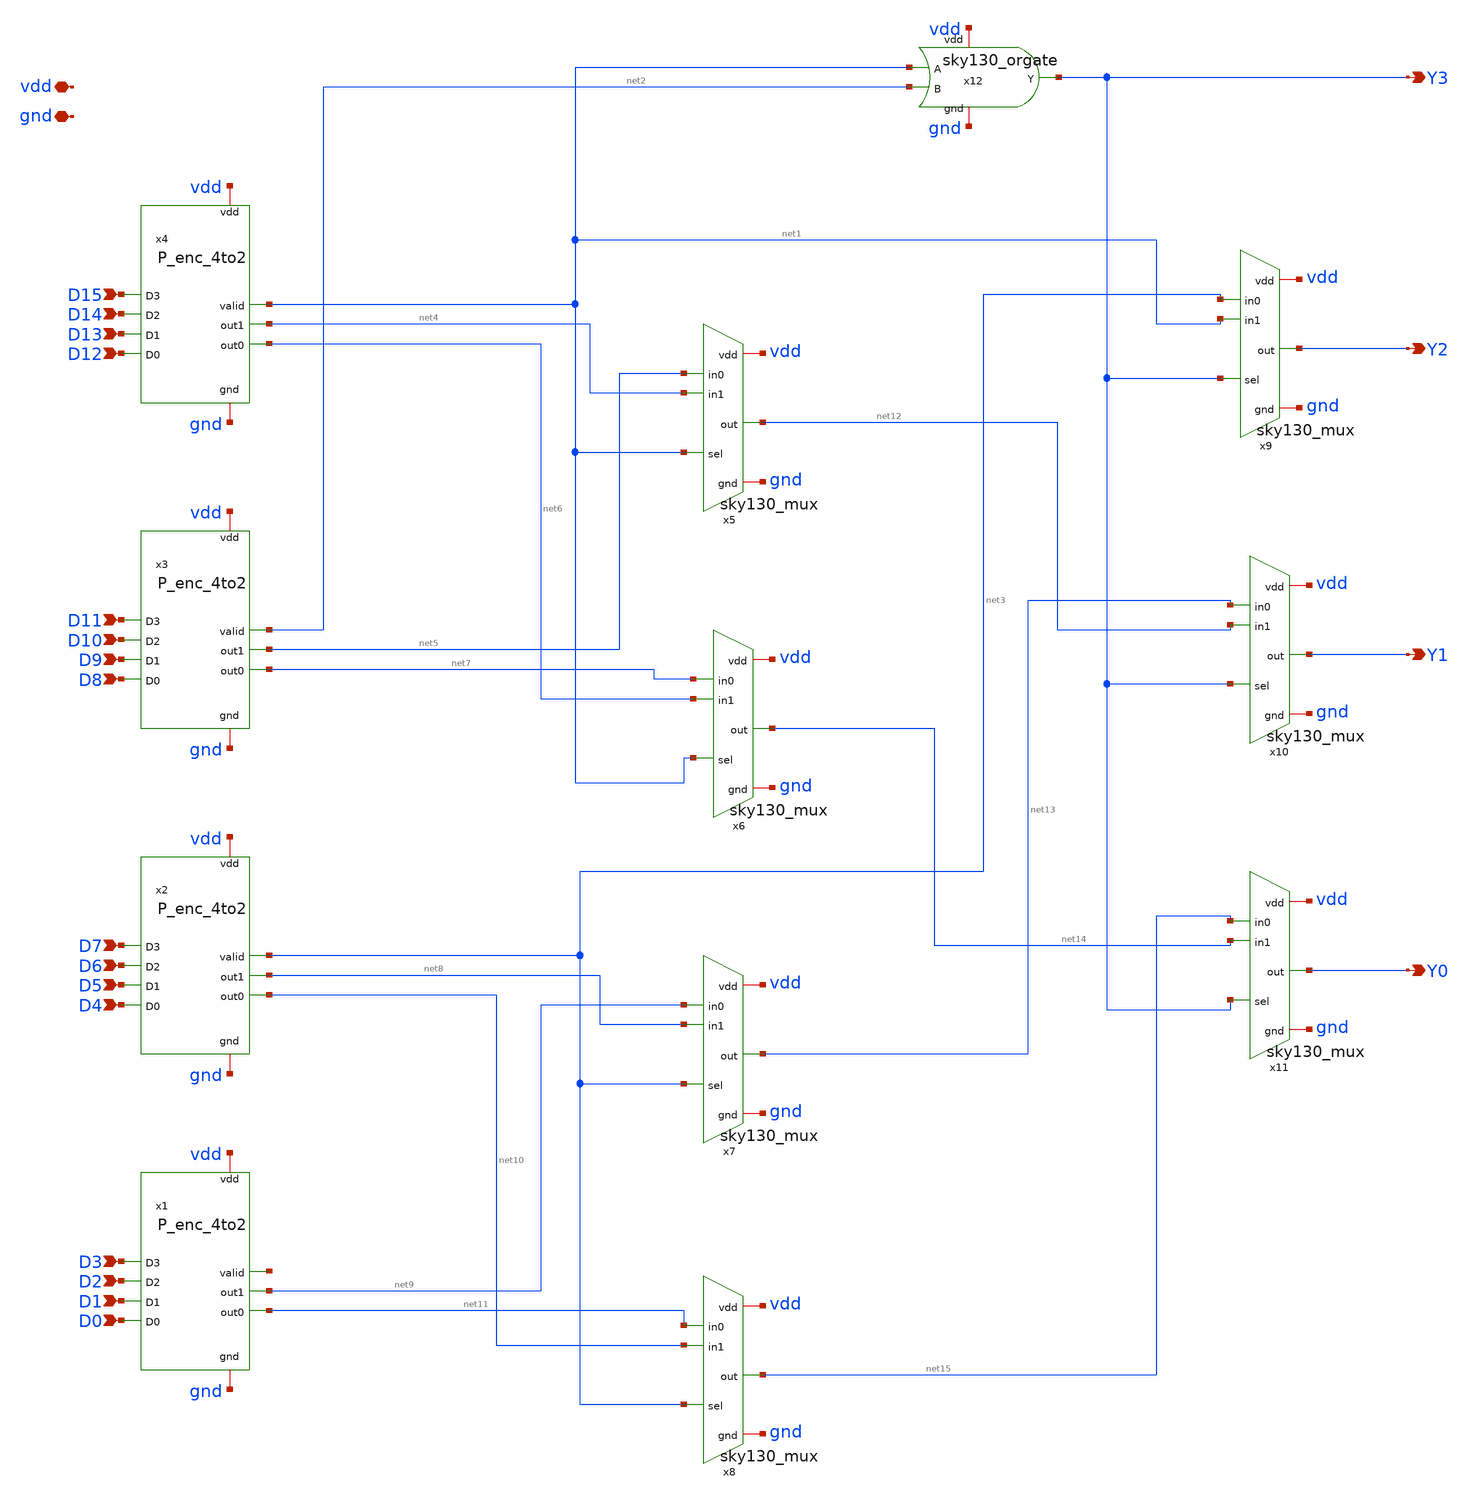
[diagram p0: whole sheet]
** sch_path: Primitives/Priority Encoder 16to4/Xschem Files/P_enc_16to4.sch
**.subckt P_enc_16to4 vdd gnd D0 D1 D2 D3 D4 D5 D6 D7 D8 D9 D10 D11 D12 D13 D14 D15 Y0 Y1 Y2 Y3
*.iopin vdd
*.iopin gnd
*.ipin D0
*.ipin D1
*.ipin D2
*.ipin D3
*.ipin D4
*.ipin D5
*.ipin D6
*.ipin D7
*.ipin D8
*.ipin D9
*.ipin D10
*.ipin D11
*.ipin D12
*.ipin D13
*.ipin D14
*.ipin D15
*.opin Y0
*.opin Y1
*.opin Y2
*.opin Y3
x5 net5 vdd gnd net12 net4 net1 sky130_mux
x6 net7 vdd gnd net14 net6 net1 sky130_mux
x7 net9 vdd gnd net13 net8 net3 sky130_mux
x8 net11 vdd gnd net15 net10 net3 sky130_mux
x9 net3 vdd gnd Y2 net1 Y3 sky130_mux
x10 net13 vdd gnd Y1 net12 Y3 sky130_mux
x11 net15 vdd gnd Y0 net14 Y3 sky130_mux
x12 vdd net1 net2 Y3 gnd sky130_orgate
x3 vdd D11 D10 D9 D8 net7 net2 net5 gnd P_enc_4to2
x2 vdd D7 D6 D5 D4 net10 net3 net8 gnd P_enc_4to2
x1 vdd D3 D2 D1 D0 net11 net16 net9 gnd P_enc_4to2
x4 vdd D15 D14 D13 D12 net6 net1 net4 gnd P_enc_4to2
**.ends

* expanding   symbol:  /home/rachtih/ADC trials/mux/sky130_mux.sym # of pins=6
** sym_path: Primitives/Multiplexer 2to1/Xschem Files/sky130_mux.sym
** sch_path: Primitives/Multiplexer 2to1/Xschem Files/sky130_mux.sch
.subckt sky130_mux in0 vdd gnd out in1 sel
*.iopin vdd
*.iopin gnd
*.ipin in0
*.ipin sel
*.ipin in1
*.opin out
XM1 net1 sel gnd gnd sky130_fd_pr__nfet_01v8 L=0.15 W=1 nf=1 ad='int((1 + 1)/2) * 1 / 1 * 0.29' as='int((1 + 2)/2) * 1 / 1 * 0.29'
+ pd='2*int((1 + 1)/2) * (1 / 1 + 0.29)' ps='2*int((1 + 2)/2) * (1 / 1 + 0.29)' nrd='0.29 / 1 ' nrs='0.29 / 1 '
+ sa=0 sb=0 sd=0 mult=1 m=1
XM2 net1 sel vdd vdd sky130_fd_pr__pfet_01v8 L=0.15 W=1 nf=1 ad='int((1 + 1)/2) * 1 / 1 * 0.29' as='int((1 + 2)/2) * 1 / 1 * 0.29'
+ pd='2*int((1 + 1)/2) * (1 / 1 + 0.29)' ps='2*int((1 + 2)/2) * (1 / 1 + 0.29)' nrd='0.29 / 1 ' nrs='0.29 / 1 '
+ sa=0 sb=0 sd=0 mult=1 m=1
XM3 in1 sel out gnd sky130_fd_pr__nfet_01v8 L=0.15 W=1 nf=1 ad='int((1 + 1)/2) * 1 / 1 * 0.29' as='int((1 + 2)/2) * 1 / 1 * 0.29'
+ pd='2*int((1 + 1)/2) * (1 / 1 + 0.29)' ps='2*int((1 + 2)/2) * (1 / 1 + 0.29)' nrd='0.29 / 1 ' nrs='0.29 / 1 '
+ sa=0 sb=0 sd=0 mult=1 m=1
XM4 in1 net1 out vdd sky130_fd_pr__pfet_01v8 L=0.15 W=1 nf=1 ad='int((1 + 1)/2) * 1 / 1 * 0.29' as='int((1 + 2)/2) * 1 / 1 * 0.29'
+ pd='2*int((1 + 1)/2) * (1 / 1 + 0.29)' ps='2*int((1 + 2)/2) * (1 / 1 + 0.29)' nrd='0.29 / 1 ' nrs='0.29 / 1 '
+ sa=0 sb=0 sd=0 mult=1 m=1
XM5 in0 net1 out gnd sky130_fd_pr__nfet_01v8 L=0.15 W=1 nf=1 ad='int((1 + 1)/2) * 1 / 1 * 0.29' as='int((1 + 2)/2) * 1 / 1 * 0.29'
+ pd='2*int((1 + 1)/2) * (1 / 1 + 0.29)' ps='2*int((1 + 2)/2) * (1 / 1 + 0.29)' nrd='0.29 / 1 ' nrs='0.29 / 1 '
+ sa=0 sb=0 sd=0 mult=1 m=1
XM6 in0 sel out vdd sky130_fd_pr__pfet_01v8 L=0.15 W=1 nf=1 ad='int((1 + 1)/2) * 1 / 1 * 0.29' as='int((1 + 2)/2) * 1 / 1 * 0.29'
+ pd='2*int((1 + 1)/2) * (1 / 1 + 0.29)' ps='2*int((1 + 2)/2) * (1 / 1 + 0.29)' nrd='0.29 / 1 ' nrs='0.29 / 1 '
+ sa=0 sb=0 sd=0 mult=1 m=1
.ends


* expanding   symbol:  /home/rachtih/ADC trials/or_gate/sky130_orgate.sym # of pins=5
** sym_path: Primitives/OR Gate/Xschem Files/sky130_orgate.sym
** sch_path: Primitives/OR Gate/Xschem Files/sky130_orgate.sch
.subckt sky130_orgate vdd A B Y gnd
*.ipin A
*.ipin B
*.iopin gnd
*.iopin vdd
*.opin Y
XM1 net1 B gnd gnd sky130_fd_pr__nfet_01v8 L=0.15 W=1 nf=1 ad='int((1 + 1)/2) * 1 / 1 * 0.29' as='int((1 + 2)/2) * 1 / 1 * 0.29'
+ pd='2*int((1 + 1)/2) * (1 / 1 + 0.29)' ps='2*int((1 + 2)/2) * (1 / 1 + 0.29)' nrd='0.29 / 1 ' nrs='0.29 / 1 '
+ sa=0 sb=0 sd=0 mult=1 m=1
XM2 net2 A vdd vdd sky130_fd_pr__pfet_01v8 L=0.15 W=1 nf=1 ad='int((1 + 1)/2) * 1 / 1 * 0.29' as='int((1 + 2)/2) * 1 / 1 * 0.29'
+ pd='2*int((1 + 1)/2) * (1 / 1 + 0.29)' ps='2*int((1 + 2)/2) * (1 / 1 + 0.29)' nrd='0.29 / 1 ' nrs='0.29 / 1 '
+ sa=0 sb=0 sd=0 mult=1 m=1
XM3 net1 A gnd gnd sky130_fd_pr__nfet_01v8 L=0.15 W=1 nf=1 ad='int((1 + 1)/2) * 1 / 1 * 0.29' as='int((1 + 2)/2) * 1 / 1 * 0.29'
+ pd='2*int((1 + 1)/2) * (1 / 1 + 0.29)' ps='2*int((1 + 2)/2) * (1 / 1 + 0.29)' nrd='0.29 / 1 ' nrs='0.29 / 1 '
+ sa=0 sb=0 sd=0 mult=1 m=1
XM4 net1 B net2 vdd sky130_fd_pr__pfet_01v8 L=0.15 W=1 nf=1 ad='int((1 + 1)/2) * 1 / 1 * 0.29' as='int((1 + 2)/2) * 1 / 1 * 0.29'
+ pd='2*int((1 + 1)/2) * (1 / 1 + 0.29)' ps='2*int((1 + 2)/2) * (1 / 1 + 0.29)' nrd='0.29 / 1 ' nrs='0.29 / 1 '
+ sa=0 sb=0 sd=0 mult=1 m=1
XM5 Y net1 vdd vdd sky130_fd_pr__pfet_01v8 L=0.15 W=1 nf=1 ad='int((1 + 1)/2) * 1 / 1 * 0.29' as='int((1 + 2)/2) * 1 / 1 * 0.29'
+ pd='2*int((1 + 1)/2) * (1 / 1 + 0.29)' ps='2*int((1 + 2)/2) * (1 / 1 + 0.29)' nrd='0.29 / 1 ' nrs='0.29 / 1 '
+ sa=0 sb=0 sd=0 mult=1 m=1
XM6 Y net1 gnd gnd sky130_fd_pr__nfet_01v8 L=0.15 W=1 nf=1 ad='int((1 + 1)/2) * 1 / 1 * 0.29' as='int((1 + 2)/2) * 1 / 1 * 0.29'
+ pd='2*int((1 + 1)/2) * (1 / 1 + 0.29)' ps='2*int((1 + 2)/2) * (1 / 1 + 0.29)' nrd='0.29 / 1 ' nrs='0.29 / 1 '
+ sa=0 sb=0 sd=0 mult=1 m=1
.ends


* expanding   symbol:  /home/rachtih/ADC trials/P_enc/P_enc_4to2.sym # of pins=9
** sym_path: Primitives/Priority Encoder 4to2/Xschem Files/P_enc_4to2.sym
** sch_path: Primitives/Priority Encoder 4to2/Xschem Files/P_enc_4to2.sch
.subckt P_enc_4to2 vdd D3 D2 D1 D0 out0 valid out1 gnd
*.opin valid
*.iopin vdd
*.iopin gnd
*.opin out1
*.opin out0
*.ipin D3
*.ipin D2
*.ipin D1
*.ipin D0
XM5 net7 D3 vdd vdd sky130_fd_pr__pfet_01v8 L=0.15 W=1 nf=1 ad='int((1 + 1)/2) * 1 / 1 * 0.29' as='int((1 + 2)/2) * 1 / 1 * 0.29'
+ pd='2*int((1 + 1)/2) * (1 / 1 + 0.29)' ps='2*int((1 + 2)/2) * (1 / 1 + 0.29)' nrd='0.29 / 1 ' nrs='0.29 / 1 '
+ sa=0 sb=0 sd=0 mult=1 m=1
XM6 net8 D2 net7 vdd sky130_fd_pr__pfet_01v8 L=0.15 W=1 nf=1 ad='int((1 + 1)/2) * 1 / 1 * 0.29' as='int((1 + 2)/2) * 1 / 1 * 0.29'
+ pd='2*int((1 + 1)/2) * (1 / 1 + 0.29)' ps='2*int((1 + 2)/2) * (1 / 1 + 0.29)' nrd='0.29 / 1 ' nrs='0.29 / 1 '
+ sa=0 sb=0 sd=0 mult=1 m=1
XM7 net9 D1 net8 vdd sky130_fd_pr__pfet_01v8 L=0.15 W=1 nf=1 ad='int((1 + 1)/2) * 1 / 1 * 0.29' as='int((1 + 2)/2) * 1 / 1 * 0.29'
+ pd='2*int((1 + 1)/2) * (1 / 1 + 0.29)' ps='2*int((1 + 2)/2) * (1 / 1 + 0.29)' nrd='0.29 / 1 ' nrs='0.29 / 1 '
+ sa=0 sb=0 sd=0 mult=1 m=1
XM8 net1 D0 net9 vdd sky130_fd_pr__pfet_01v8 L=0.15 W=1 nf=1 ad='int((1 + 1)/2) * 1 / 1 * 0.29' as='int((1 + 2)/2) * 1 / 1 * 0.29'
+ pd='2*int((1 + 1)/2) * (1 / 1 + 0.29)' ps='2*int((1 + 2)/2) * (1 / 1 + 0.29)' nrd='0.29 / 1 ' nrs='0.29 / 1 '
+ sa=0 sb=0 sd=0 mult=1 m=1
XM9 net1 D0 gnd gnd sky130_fd_pr__nfet_01v8 L=0.15 W=1 nf=1 ad='int((1 + 1)/2) * 1 / 1 * 0.29' as='int((1 + 2)/2) * 1 / 1 * 0.29'
+ pd='2*int((1 + 1)/2) * (1 / 1 + 0.29)' ps='2*int((1 + 2)/2) * (1 / 1 + 0.29)' nrd='0.29 / 1 ' nrs='0.29 / 1 '
+ sa=0 sb=0 sd=0 mult=1 m=1
XM10 net1 D1 gnd gnd sky130_fd_pr__nfet_01v8 L=0.15 W=1 nf=1 ad='int((1 + 1)/2) * 1 / 1 * 0.29' as='int((1 + 2)/2) * 1 / 1 * 0.29'
+ pd='2*int((1 + 1)/2) * (1 / 1 + 0.29)' ps='2*int((1 + 2)/2) * (1 / 1 + 0.29)' nrd='0.29 / 1 ' nrs='0.29 / 1 '
+ sa=0 sb=0 sd=0 mult=1 m=1
XM11 net1 D2 gnd gnd sky130_fd_pr__nfet_01v8 L=0.15 W=1 nf=1 ad='int((1 + 1)/2) * 1 / 1 * 0.29' as='int((1 + 2)/2) * 1 / 1 * 0.29'
+ pd='2*int((1 + 1)/2) * (1 / 1 + 0.29)' ps='2*int((1 + 2)/2) * (1 / 1 + 0.29)' nrd='0.29 / 1 ' nrs='0.29 / 1 '
+ sa=0 sb=0 sd=0 mult=1 m=1
XM12 net1 D3 gnd gnd sky130_fd_pr__nfet_01v8 L=0.15 W=1 nf=1 ad='int((1 + 1)/2) * 1 / 1 * 0.29' as='int((1 + 2)/2) * 1 / 1 * 0.29'
+ pd='2*int((1 + 1)/2) * (1 / 1 + 0.29)' ps='2*int((1 + 2)/2) * (1 / 1 + 0.29)' nrd='0.29 / 1 ' nrs='0.29 / 1 '
+ sa=0 sb=0 sd=0 mult=1 m=1
XM13 valid net1 gnd gnd sky130_fd_pr__nfet_01v8 L=0.15 W=1 nf=1 ad='int((1 + 1)/2) * 1 / 1 * 0.29' as='int((1 + 2)/2) * 1 / 1 * 0.29'
+ pd='2*int((1 + 1)/2) * (1 / 1 + 0.29)' ps='2*int((1 + 2)/2) * (1 / 1 + 0.29)' nrd='0.29 / 1 ' nrs='0.29 / 1 '
+ sa=0 sb=0 sd=0 mult=1 m=1
XM14 valid net1 vdd vdd sky130_fd_pr__pfet_01v8 L=0.15 W=1 nf=1 ad='int((1 + 1)/2) * 1 / 1 * 0.29' as='int((1 + 2)/2) * 1 / 1 * 0.29'
+ pd='2*int((1 + 1)/2) * (1 / 1 + 0.29)' ps='2*int((1 + 2)/2) * (1 / 1 + 0.29)' nrd='0.29 / 1 ' nrs='0.29 / 1 '
+ sa=0 sb=0 sd=0 mult=1 m=1
XM17 net2 D2 gnd gnd sky130_fd_pr__nfet_01v8 L=0.15 W=1 nf=1 ad='int((1 + 1)/2) * 1 / 1 * 0.29' as='int((1 + 2)/2) * 1 / 1 * 0.29'
+ pd='2*int((1 + 1)/2) * (1 / 1 + 0.29)' ps='2*int((1 + 2)/2) * (1 / 1 + 0.29)' nrd='0.29 / 1 ' nrs='0.29 / 1 '
+ sa=0 sb=0 sd=0 mult=1 m=1
XM18 net2 D2 vdd vdd sky130_fd_pr__pfet_01v8 L=0.15 W=1 nf=1 ad='int((1 + 1)/2) * 1 / 1 * 0.29' as='int((1 + 2)/2) * 1 / 1 * 0.29'
+ pd='2*int((1 + 1)/2) * (1 / 1 + 0.29)' ps='2*int((1 + 2)/2) * (1 / 1 + 0.29)' nrd='0.29 / 1 ' nrs='0.29 / 1 '
+ sa=0 sb=0 sd=0 mult=1 m=1
XM19 net4 D3 vdd vdd sky130_fd_pr__pfet_01v8 L=0.15 W=1 nf=1 ad='int((1 + 1)/2) * 1 / 1 * 0.29' as='int((1 + 2)/2) * 1 / 1 * 0.29'
+ pd='2*int((1 + 1)/2) * (1 / 1 + 0.29)' ps='2*int((1 + 2)/2) * (1 / 1 + 0.29)' nrd='0.29 / 1 ' nrs='0.29 / 1 '
+ sa=0 sb=0 sd=0 mult=1 m=1
XM20 net3 net2 net4 vdd sky130_fd_pr__pfet_01v8 L=0.15 W=1 nf=1 ad='int((1 + 1)/2) * 1 / 1 * 0.29' as='int((1 + 2)/2) * 1 / 1 * 0.29'
+ pd='2*int((1 + 1)/2) * (1 / 1 + 0.29)' ps='2*int((1 + 2)/2) * (1 / 1 + 0.29)' nrd='0.29 / 1 ' nrs='0.29 / 1 '
+ sa=0 sb=0 sd=0 mult=1 m=1
XM21 net3 D1 net4 vdd sky130_fd_pr__pfet_01v8 L=0.15 W=1 nf=1 ad='int((1 + 1)/2) * 1 / 1 * 0.29' as='int((1 + 2)/2) * 1 / 1 * 0.29'
+ pd='2*int((1 + 1)/2) * (1 / 1 + 0.29)' ps='2*int((1 + 2)/2) * (1 / 1 + 0.29)' nrd='0.29 / 1 ' nrs='0.29 / 1 '
+ sa=0 sb=0 sd=0 mult=1 m=1
XM22 net3 D3 gnd gnd sky130_fd_pr__nfet_01v8 L=0.15 W=1 nf=1 ad='int((1 + 1)/2) * 1 / 1 * 0.29' as='int((1 + 2)/2) * 1 / 1 * 0.29'
+ pd='2*int((1 + 1)/2) * (1 / 1 + 0.29)' ps='2*int((1 + 2)/2) * (1 / 1 + 0.29)' nrd='0.29 / 1 ' nrs='0.29 / 1 '
+ sa=0 sb=0 sd=0 mult=1 m=1
XM23 net3 net2 net10 gnd sky130_fd_pr__nfet_01v8 L=0.15 W=1 nf=1 ad='int((1 + 1)/2) * 1 / 1 * 0.29' as='int((1 + 2)/2) * 1 / 1 * 0.29'
+ pd='2*int((1 + 1)/2) * (1 / 1 + 0.29)' ps='2*int((1 + 2)/2) * (1 / 1 + 0.29)' nrd='0.29 / 1 ' nrs='0.29 / 1 '
+ sa=0 sb=0 sd=0 mult=1 m=1
XM24 net10 D1 gnd gnd sky130_fd_pr__nfet_01v8 L=0.15 W=1 nf=1 ad='int((1 + 1)/2) * 1 / 1 * 0.29' as='int((1 + 2)/2) * 1 / 1 * 0.29'
+ pd='2*int((1 + 1)/2) * (1 / 1 + 0.29)' ps='2*int((1 + 2)/2) * (1 / 1 + 0.29)' nrd='0.29 / 1 ' nrs='0.29 / 1 '
+ sa=0 sb=0 sd=0 mult=1 m=1
XM25 out0 net3 vdd vdd sky130_fd_pr__pfet_01v8 L=0.15 W=1 nf=1 ad='int((1 + 1)/2) * 1 / 1 * 0.29' as='int((1 + 2)/2) * 1 / 1 * 0.29'
+ pd='2*int((1 + 1)/2) * (1 / 1 + 0.29)' ps='2*int((1 + 2)/2) * (1 / 1 + 0.29)' nrd='0.29 / 1 ' nrs='0.29 / 1 '
+ sa=0 sb=0 sd=0 mult=1 m=1
XM26 out0 net3 gnd gnd sky130_fd_pr__nfet_01v8 L=0.15 W=1 nf=1 ad='int((1 + 1)/2) * 1 / 1 * 0.29' as='int((1 + 2)/2) * 1 / 1 * 0.29'
+ pd='2*int((1 + 1)/2) * (1 / 1 + 0.29)' ps='2*int((1 + 2)/2) * (1 / 1 + 0.29)' nrd='0.29 / 1 ' nrs='0.29 / 1 '
+ sa=0 sb=0 sd=0 mult=1 m=1
XM1 net5 D3 gnd gnd sky130_fd_pr__nfet_01v8 L=0.15 W=1 nf=1 ad='int((1 + 1)/2) * 1 / 1 * 0.29' as='int((1 + 2)/2) * 1 / 1 * 0.29'
+ pd='2*int((1 + 1)/2) * (1 / 1 + 0.29)' ps='2*int((1 + 2)/2) * (1 / 1 + 0.29)' nrd='0.29 / 1 ' nrs='0.29 / 1 '
+ sa=0 sb=0 sd=0 mult=1 m=1
XM2 net5 D2 net6 vdd sky130_fd_pr__pfet_01v8 L=0.15 W=1 nf=1 ad='int((1 + 1)/2) * 1 / 1 * 0.29' as='int((1 + 2)/2) * 1 / 1 * 0.29'
+ pd='2*int((1 + 1)/2) * (1 / 1 + 0.29)' ps='2*int((1 + 2)/2) * (1 / 1 + 0.29)' nrd='0.29 / 1 ' nrs='0.29 / 1 '
+ sa=0 sb=0 sd=0 mult=1 m=1
XM3 net6 D3 vdd vdd sky130_fd_pr__pfet_01v8 L=0.15 W=1 nf=1 ad='int((1 + 1)/2) * 1 / 1 * 0.29' as='int((1 + 2)/2) * 1 / 1 * 0.29'
+ pd='2*int((1 + 1)/2) * (1 / 1 + 0.29)' ps='2*int((1 + 2)/2) * (1 / 1 + 0.29)' nrd='0.29 / 1 ' nrs='0.29 / 1 '
+ sa=0 sb=0 sd=0 mult=1 m=1
XM4 net5 D2 gnd gnd sky130_fd_pr__nfet_01v8 L=0.15 W=1 nf=1 ad='int((1 + 1)/2) * 1 / 1 * 0.29' as='int((1 + 2)/2) * 1 / 1 * 0.29'
+ pd='2*int((1 + 1)/2) * (1 / 1 + 0.29)' ps='2*int((1 + 2)/2) * (1 / 1 + 0.29)' nrd='0.29 / 1 ' nrs='0.29 / 1 '
+ sa=0 sb=0 sd=0 mult=1 m=1
XM15 out1 net5 gnd gnd sky130_fd_pr__nfet_01v8 L=0.15 W=1 nf=1 ad='int((1 + 1)/2) * 1 / 1 * 0.29' as='int((1 + 2)/2) * 1 / 1 * 0.29'
+ pd='2*int((1 + 1)/2) * (1 / 1 + 0.29)' ps='2*int((1 + 2)/2) * (1 / 1 + 0.29)' nrd='0.29 / 1 ' nrs='0.29 / 1 '
+ sa=0 sb=0 sd=0 mult=1 m=1
XM16 out1 net5 vdd vdd sky130_fd_pr__pfet_01v8 L=0.15 W=1 nf=1 ad='int((1 + 1)/2) * 1 / 1 * 0.29' as='int((1 + 2)/2) * 1 / 1 * 0.29'
+ pd='2*int((1 + 1)/2) * (1 / 1 + 0.29)' ps='2*int((1 + 2)/2) * (1 / 1 + 0.29)' nrd='0.29 / 1 ' nrs='0.29 / 1 '
+ sa=0 sb=0 sd=0 mult=1 m=1
.ends

.end
